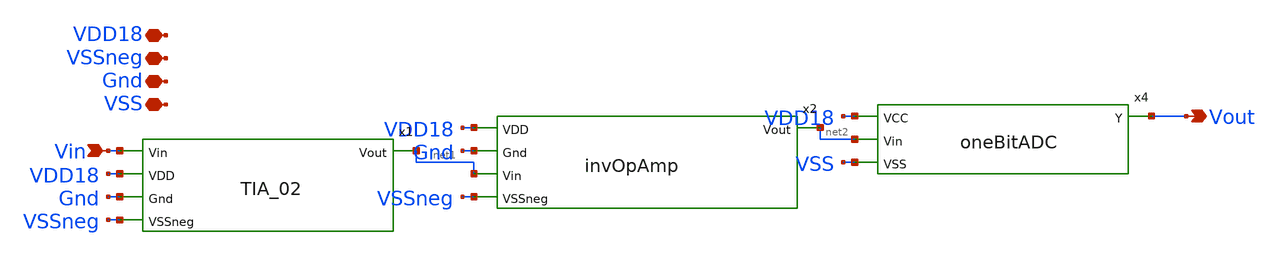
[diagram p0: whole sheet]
** sch_path: xschem/1LineSelectOutput02.sch
**.subckt 1LineSelectOutput02 Vin VDD18 Vout VSSneg Gnd VSS
*.ipin Vin
*.iopin VDD18
*.opin Vout
*.iopin VSSneg
*.iopin Gnd
*.iopin VSS
x4 VDD18 Vout net2 VSS oneBitADC
x1 Vin VDD18 net1 Gnd VSSneg TIA_02
x2 net2 VDD18 Gnd net1 VSSneg invOpAmp
**.ends
.end
